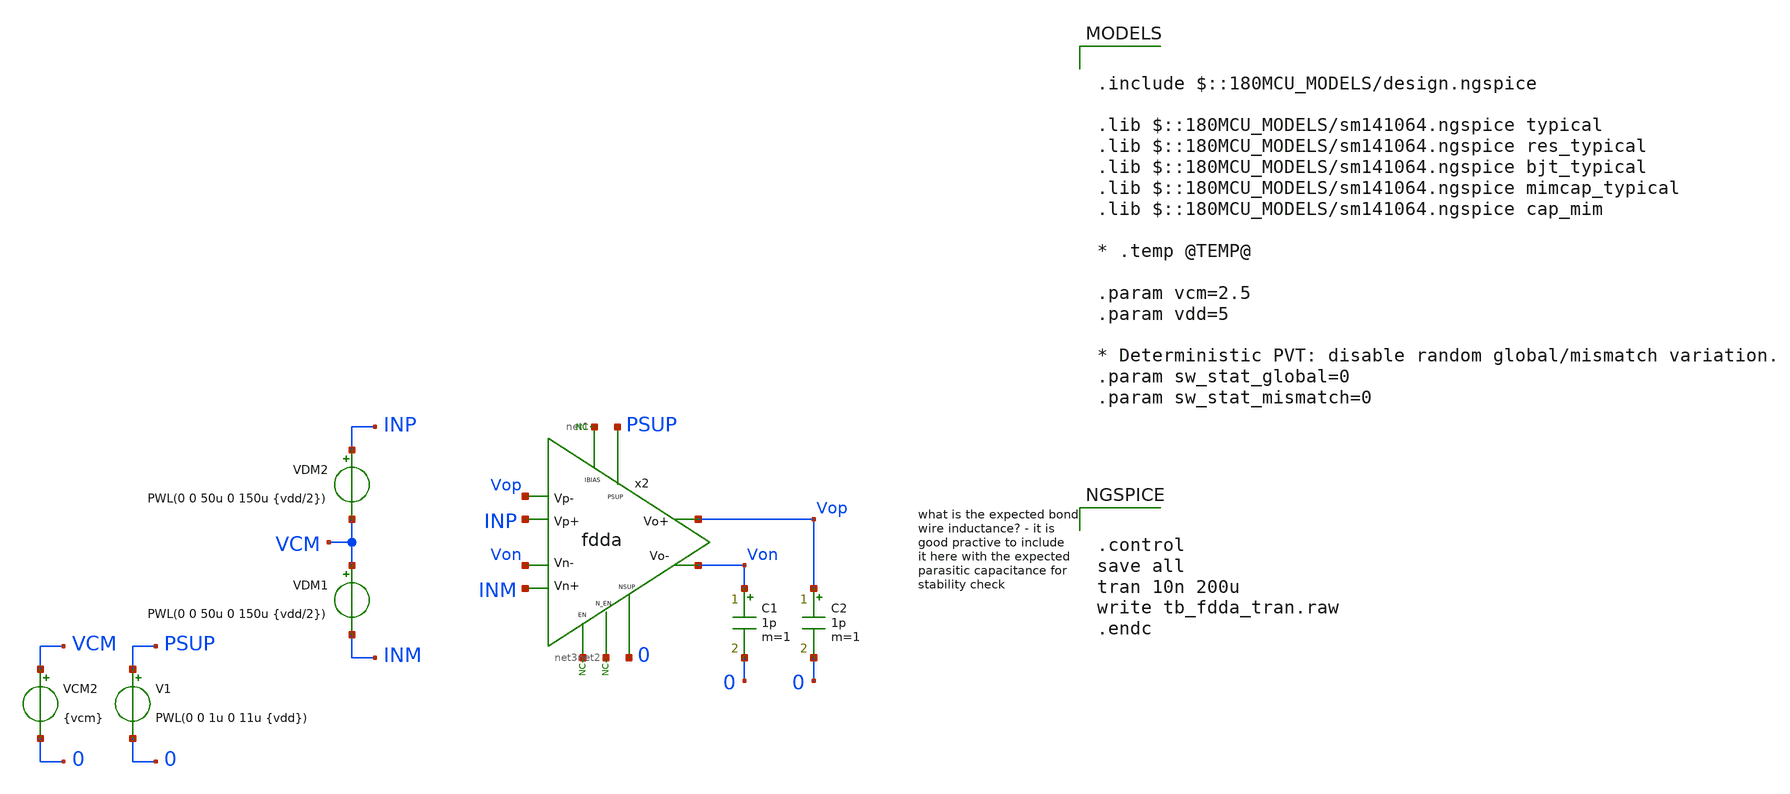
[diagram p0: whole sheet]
** sch_path: xschem/blocks/fdda/tb_fdda_tran.sch
**.subckt tb_fdda_tran
C1 Von 0 1p m=1
x2 PSUP Vop Von INM INP Vop Von net1 net2 net3 0 fdda
* noconn #net1
* noconn #net3
* noconn #net2
V1 PSUP 0 PWL(0 0 1u 0 11u {vdd})
C2 Vop 0 1p m=1
VCM2 VCM 0 {vcm}
VDM2 INP VCM PWL(0 0 50u 0 150u {vdd/2})
VDM1 VCM INM PWL(0 0 50u 0 150u {vdd/2})
**** begin user architecture code

.include $::180MCU_MODELS/design.ngspice

.lib $::180MCU_MODELS/sm141064.ngspice typical
.lib $::180MCU_MODELS/sm141064.ngspice res_typical
.lib $::180MCU_MODELS/sm141064.ngspice bjt_typical
.lib $::180MCU_MODELS/sm141064.ngspice mimcap_typical
.lib $::180MCU_MODELS/sm141064.ngspice cap_mim

* .temp @TEMP@

.param vcm=2.5
.param vdd=5

* Deterministic PVT: disable random global/mismatch variation.
.param sw_stat_global=0
.param sw_stat_mismatch=0



.control
save all
tran 10n 200u
write tb_fdda_tran.raw
.endc


**** end user architecture code
**.ends

* expanding   symbol:  blocks/fdda/fdda.sym # of pins=11
** sym_path: xschem/blocks/fdda/fdda.sym
** sch_path: xschem/blocks/fdda/fdda.sch
.subckt fdda PSUP Vp- Vn+ Vn- Vp+ Vo+ Vo- IBIAS N_EN EN NSUP
*.ipin PSUP
*.ipin NSUP
*.ipin N_EN
*.ipin EN
*.ipin IBIAS
*.ipin Vp+
*.ipin Vp-
*.ipin Vn+
*.ipin Vn-
*.opin Vo+
*.opin Vo-
* noconn N_EN
* noconn EN
I0 net5 NSUP 1u
XM9 Vo+ Vp- net1 NSUP pfet_06v0 L=2u W=4u nf=5 ad='int((nf+1)/2) * W/nf * 0.18u' as='int((nf+2)/2) * W/nf * 0.18u'
+ pd='2*int((nf+1)/2) * (W/nf + 0.18u)' ps='2*int((nf+2)/2) * (W/nf + 0.18u)' nrd='0.18u / W' nrs='0.18u / W'
+ sa=0 sb=0 sd=0 m=10
XM1 Vo- Vp+ net1 NSUP pfet_06v0 L=2u W=4u nf=5 ad='int((nf+1)/2) * W/nf * 0.18u' as='int((nf+2)/2) * W/nf * 0.18u'
+ pd='2*int((nf+1)/2) * (W/nf + 0.18u)' ps='2*int((nf+2)/2) * (W/nf + 0.18u)' nrd='0.18u / W' nrs='0.18u / W'
+ sa=0 sb=0 sd=0 m=10
XM2 net1 vb1 PSUP net3 pfet_06v0 L=4u W=2u nf=1 ad='int((nf+1)/2) * W/nf * 0.18u' as='int((nf+2)/2) * W/nf * 0.18u'
+ pd='2*int((nf+1)/2) * (W/nf + 0.18u)' ps='2*int((nf+2)/2) * (W/nf + 0.18u)' nrd='0.18u / W' nrs='0.18u / W'
+ sa=0 sb=0 sd=0 m=8
XM3 Vo- Vo- NSUP NSUP nfet_06v0 L=4u W=2u nf=1 ad='int((nf+1)/2) * W/nf * 0.18u' as='int((nf+2)/2) * W/nf * 0.18u'
+ pd='2*int((nf+1)/2) * (W/nf + 0.18u)' ps='2*int((nf+2)/2) * (W/nf + 0.18u)' nrd='0.18u / W' nrs='0.18u / W'
+ sa=0 sb=0 sd=0 m=4
XM4 Vo+ Vn- net2 NSUP pfet_06v0 L=2u W=4u nf=5 ad='int((nf+1)/2) * W/nf * 0.18u' as='int((nf+2)/2) * W/nf * 0.18u'
+ pd='2*int((nf+1)/2) * (W/nf + 0.18u)' ps='2*int((nf+2)/2) * (W/nf + 0.18u)' nrd='0.18u / W' nrs='0.18u / W'
+ sa=0 sb=0 sd=0 m=10
XM5 Vo- Vn+ net2 NSUP pfet_06v0 L=2u W=4u nf=5 ad='int((nf+1)/2) * W/nf * 0.18u' as='int((nf+2)/2) * W/nf * 0.18u'
+ pd='2*int((nf+1)/2) * (W/nf + 0.18u)' ps='2*int((nf+2)/2) * (W/nf + 0.18u)' nrd='0.18u / W' nrs='0.18u / W'
+ sa=0 sb=0 sd=0 m=10
XM6 net2 vb1 PSUP PSUP pfet_06v0 L=4u W=2u nf=1 ad='int((nf+1)/2) * W/nf * 0.18u' as='int((nf+2)/2) * W/nf * 0.18u'
+ pd='2*int((nf+1)/2) * (W/nf + 0.18u)' ps='2*int((nf+2)/2) * (W/nf + 0.18u)' nrd='0.18u / W' nrs='0.18u / W'
+ sa=0 sb=0 sd=0 m=8
XM8 Vo+ Vo+ NSUP NSUP nfet_06v0 L=4u W=2u nf=1 ad='int((nf+1)/2) * W/nf * 0.18u' as='int((nf+2)/2) * W/nf * 0.18u'
+ pd='2*int((nf+1)/2) * (W/nf + 0.18u)' ps='2*int((nf+2)/2) * (W/nf + 0.18u)' nrd='0.18u / W' nrs='0.18u / W'
+ sa=0 sb=0 sd=0 m=4
XM7 net5 vb1 PSUP net4 pfet_06v0 L=4u W=2u nf=1 ad='int((nf+1)/2) * W/nf * 0.18u' as='int((nf+2)/2) * W/nf * 0.18u'
+ pd='2*int((nf+1)/2) * (W/nf + 0.18u)' ps='2*int((nf+2)/2) * (W/nf + 0.18u)' nrd='0.18u / W' nrs='0.18u / W'
+ sa=0 sb=0 sd=0 m=4
.ends

.end
